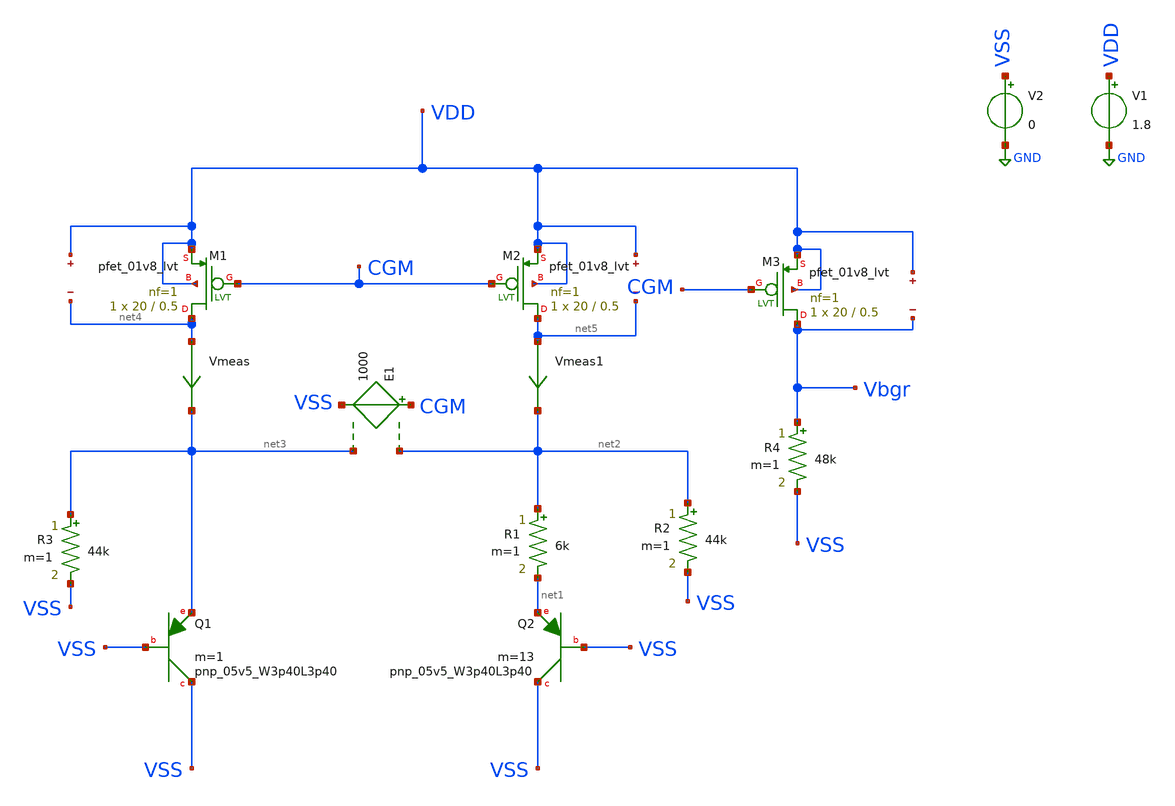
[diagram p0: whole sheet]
** sch_path: custom_gds/tt_um_bgr_agolmanesh/xschem/BGRCore.sch
**.subckt BGRCore
XQ1 VSS VSS net3 sky130_fd_pr__pnp_05v5_W3p40L3p40 m=1
XQ2 VSS VSS net1 sky130_fd_pr__pnp_05v5_W3p40L3p40 m=13
XM1 net4 CGM VDD VDD sky130_fd_pr__pfet_01v8_lvt L=0.5 W=20 nf=1 ad='int((nf+1)/2) * W/nf * 0.29' as='int((nf+2)/2) * W/nf * 0.29'
+ pd='2*int((nf+1)/2) * (W/nf + 0.29)' ps='2*int((nf+2)/2) * (W/nf + 0.29)' nrd='0.29 / W' nrs='0.29 / W'
+ sa=0 sb=0 sd=0 mult=1 m=1
XM2 net5 CGM VDD VDD sky130_fd_pr__pfet_01v8_lvt L=0.5 W=20 nf=1 ad='int((nf+1)/2) * W/nf * 0.29' as='int((nf+2)/2) * W/nf * 0.29'
+ pd='2*int((nf+1)/2) * (W/nf + 0.29)' ps='2*int((nf+2)/2) * (W/nf + 0.29)' nrd='0.29 / W' nrs='0.29 / W'
+ sa=0 sb=0 sd=0 mult=1 m=1
XM3 Vbgr CGM VDD VDD sky130_fd_pr__pfet_01v8_lvt L=0.5 W=20 nf=1 ad='int((nf+1)/2) * W/nf * 0.29' as='int((nf+2)/2) * W/nf * 0.29'
+ pd='2*int((nf+1)/2) * (W/nf + 0.29)' ps='2*int((nf+2)/2) * (W/nf + 0.29)' nrd='0.29 / W' nrs='0.29 / W'
+ sa=0 sb=0 sd=0 mult=1 m=1
E1 CGM VSS net2 net3 1000
R1 net2 net1 6k m=1
R2 net2 VSS 44k m=1
R3 net3 VSS 44k m=1
R4 Vbgr VSS 48k m=1
V1 VDD GND 1.8
V2 VSS GND 0
Vmeas net4 net3 0
.save i(vmeas)
Vmeas1 net5 net2 0
.save i(vmeas1)
.save v(vdd)
.save v(net4)
.save v(vdd)
.save v(net5)
.save v(vdd)
.save v(vbgr)
**** begin user architecture code

** opencircuitdesign pdks install
.lib $::SKYWATER_MODELS/sky130.lib.spice tt


**** end user architecture code
**.ends
.GLOBAL GND
**** begin user architecture code



.options savecurrents
.control
save all

save @m.xm1.msky130_fd_pr__ppet_01v8_lvt[gm]
save @m.xm1.msky130_fd_pr__pfet_01v8_lvt[id]
save @m.xm1.msky130_fd_pr__pfet_01v8_lvt[vgs]
save @m.xm1.msky130_fd_pr__pfet_01v8_lvt[vds]
save @m.xm1.msky130_fd_pr__pfet_01v8_lvt[cgg]
save @m.xm1.msky130_fd_pr__pfet_01v8_lvt[vdsat]
save @m.xm1.msky130_fd_pr__pfet_01v8_lvt[vth]


save @m.xm2.msky130_fd_pr__pfet_01v8_lvt[gm]
save @m.xm2.msky130_fd_pr__pfet_01v8_lvt[id]
save @m.xm2.msky130_fd_pr__pfet_01v8_lvt[vgs]
save @m.xm2.msky130_fd_pr__pfet_01v8_lvt[vds]
save @m.xm2.msky130_fd_pr__pfet_01v8_lvt[cgg]
save @m.xm2.msky130_fd_pr__pfet_01v8_lvt[vdsat]
save @m.xm2.msky130_fd_pr__pfet_01v8_lvt[vth]


save @m.xm3.msky130_fd_pr__pfet_01v8_lvt[gm]
save @m.xm3.msky130_fd_pr__pfet_01v8_lvt[id]
save @m.xm3.msky130_fd_pr__pfet_01v8_lvt[vgs]
save @m.xm3.msky130_fd_pr__pfet_01v8_lvt[vds]
save @m.xm3.msky130_fd_pr__pfet_01v8_lvt[cgg]
save @m.xm3.msky130_fd_pr__pfet_01v8_lvt[vdsat]
save @m.xm3.msky130_fd_pr__pfet_01v8_lvt[vth]

save @q.xq1.qsky130_fd_pr__pnp_05v5_W3p40L3p40[vbe]
save @q.xq2.qsky130_fd_pr__pnp_05v5_W3p40L3p40[vbe]

op
write BGRCore.raw

dc TEMP -40 70 10
plot deriv(Vbgr)
.endc



**** end user architecture code
.end
